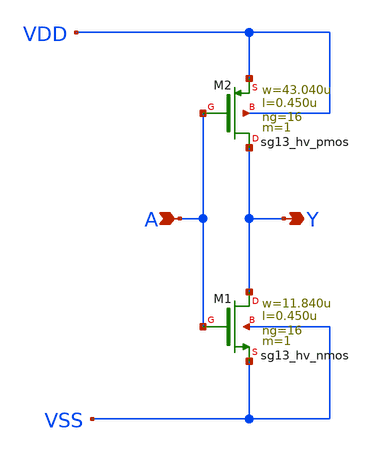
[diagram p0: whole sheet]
** sch_path: ihp-sg13g2/libs.ref/sg13g2_stdcell_hv/sch/xschem/sg13g2_hv_inv_16.sch
* Copyright 2023 IHP PDK Authors
* Licensed under the Apache License, Version 2.0 (the "License");
* you may not use this file except in compliance with the License.
* You may obtain a copy of the License at
* https://www.apache.org/licenses/LICENSE-2.0
* Unless required by applicable law or agreed to in writing, software
* distributed under the License is distributed on an "AS IS" BASIS,
* WITHOUT WARRANTIES OR CONDITIONS OF ANY KIND, either express or implied.
* See the License for the specific language governing permissions and
* limitations under the License.
**.subckt sg13g2_hv_inv_16 Y A
*.opin Y
*.ipin A
XM1 Y A VSS VSS sg13_hv_nmos w=11.840u l=0.450u ng=16 m=1 mm_ok=1
XM2 Y A VDD VDD sg13_hv_pmos w=43.040u l=0.450u ng=16 m=1 mm_ok=1
**.ends
.end
